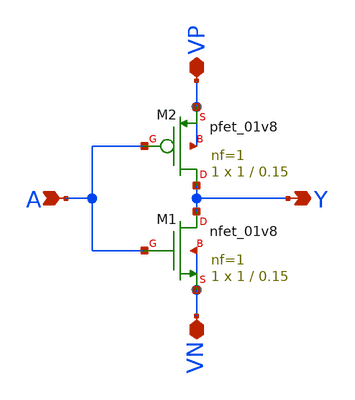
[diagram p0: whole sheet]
** sch_path: projekat_spice/layout/invertor/invertor.sch
**.subckt invertor VP VN A Y
*.iopin VP
*.iopin VN
*.ipin A
*.opin Y
XM1 Y A VN VN sky130_fd_pr__nfet_01v8 L=0.15 W=1 nf=1 ad='int((nf+1)/2) * W/nf * 0.29' as='int((nf+2)/2) * W/nf * 0.29'
+ pd='2*int((nf+1)/2) * (W/nf + 0.29)' ps='2*int((nf+2)/2) * (W/nf + 0.29)' nrd='0.29 / W' nrs='0.29 / W'
+ sa=0 sb=0 sd=0 mult=1 m=1
XM2 Y A VP VP sky130_fd_pr__pfet_01v8 L=0.15 W=1 nf=1 ad='int((nf+1)/2) * W/nf * 0.29' as='int((nf+2)/2) * W/nf * 0.29'
+ pd='2*int((nf+1)/2) * (W/nf + 0.29)' ps='2*int((nf+2)/2) * (W/nf + 0.29)' nrd='0.29 / W' nrs='0.29 / W'
+ sa=0 sb=0 sd=0 mult=1 m=1
**.ends
.end
